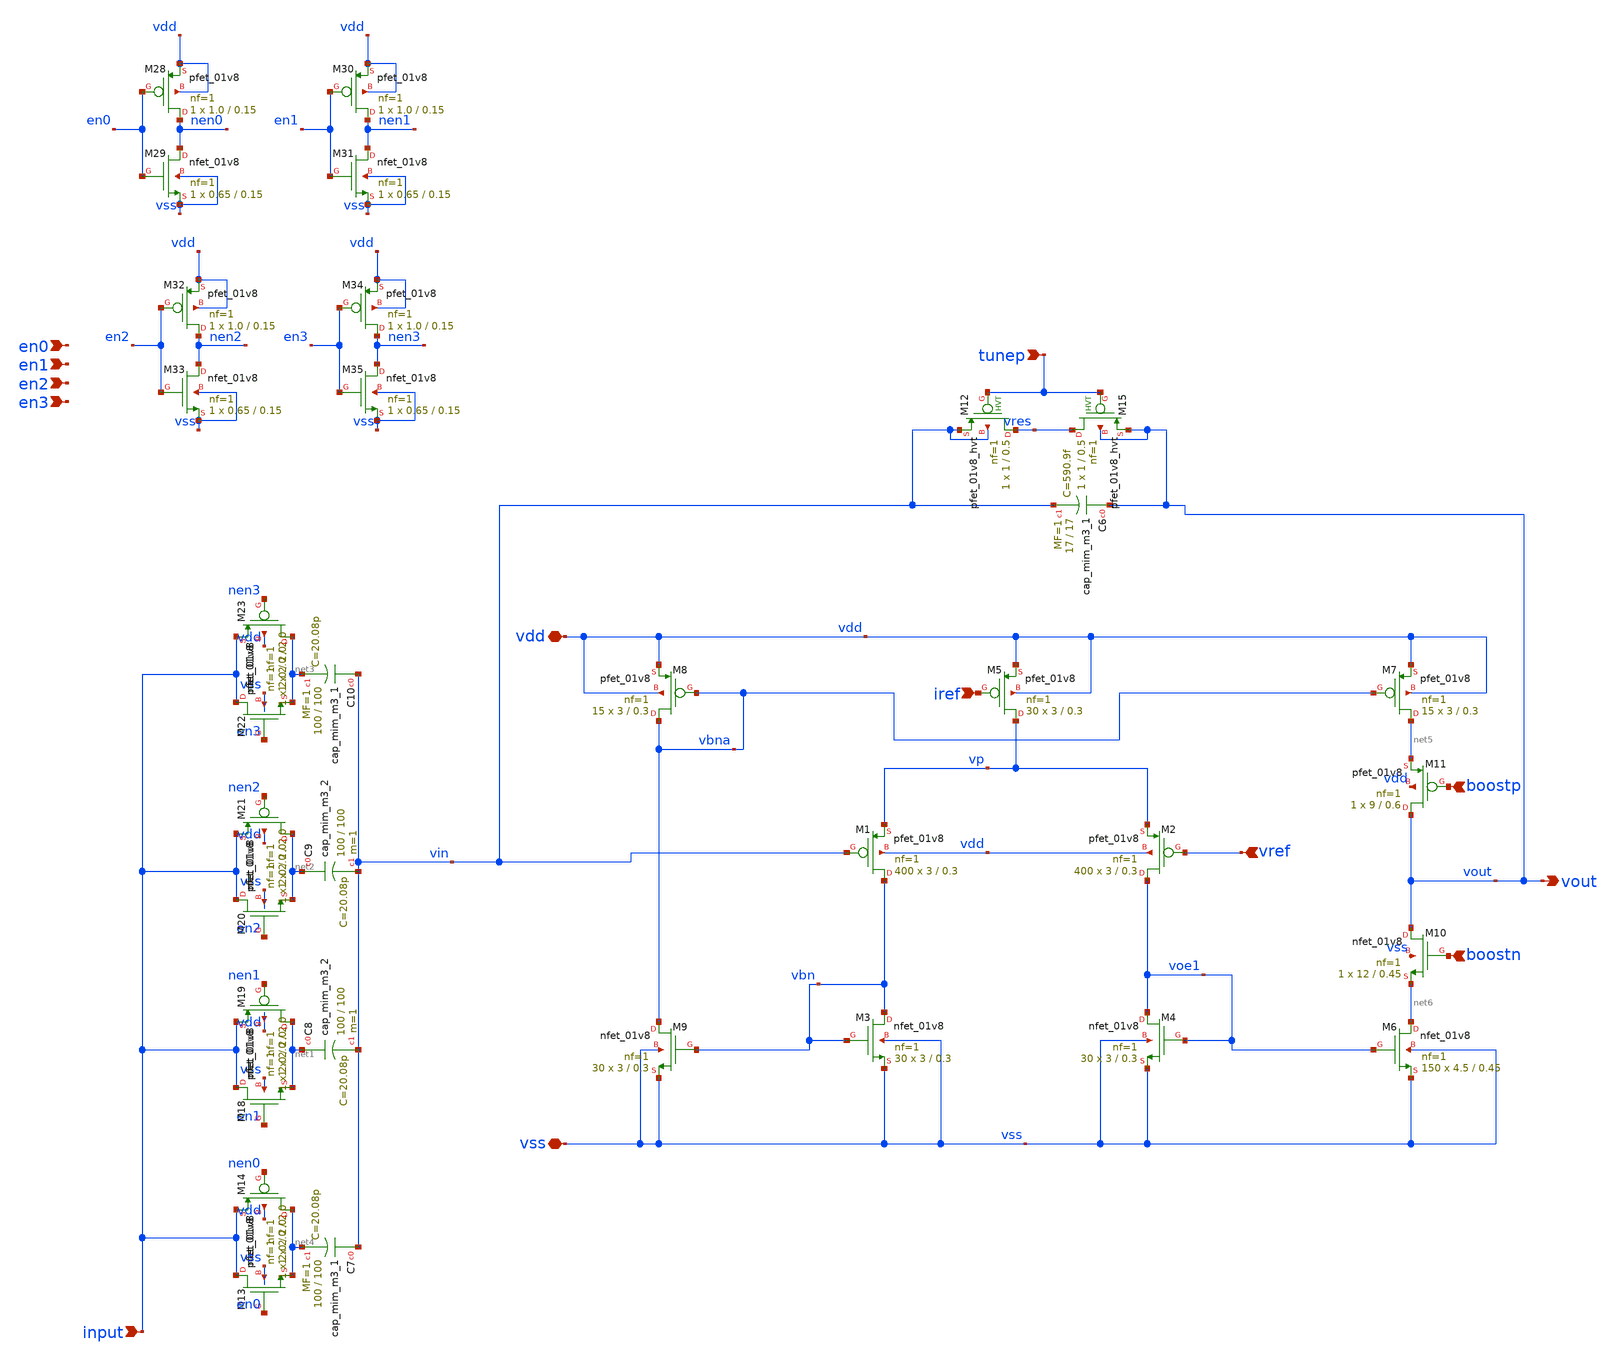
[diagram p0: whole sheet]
** sch_path: design/xschem/low_noise_amp_fc_v2.sch
**.subckt low_noise_amp_fc_v2 vdd vss vref vout iref en0 en1 en2 en3 input tunep boostp boostn
*.iopin vdd
*.iopin vss
*.ipin vref
*.opin vout
*.ipin iref
*.ipin en0
*.ipin en1
*.ipin en2
*.ipin en3
*.ipin input
*.ipin tunep
*.ipin boostp
*.ipin boostn
XM1 vbn vin vp vdd sky130_fd_pr__pfet_01v8 L=0.3 W=3 nf=1 ad='W * 0.29' as='W * 0.29' pd='2 * (W + 0.29)'
+ ps='2 * (W + 0.29)' nrd='0.29 / W' nrs='0.29 / W' sa=0 sb=0 sd=0 mult=400 m=400
XM2 voe1 vref vp vdd sky130_fd_pr__pfet_01v8 L=0.3 W=3 nf=1 ad='W * 0.29' as='W * 0.29' pd='2 * (W + 0.29)'
+ ps='2 * (W + 0.29)' nrd='0.29 / W' nrs='0.29 / W' sa=0 sb=0 sd=0 mult=400 m=400
XM3 vbn vbn vss vss sky130_fd_pr__nfet_01v8 L=0.3 W=3 nf=1 ad='W * 0.29' as='W * 0.29' pd='2 * (W + 0.29)'
+ ps='2 * (W + 0.29)' nrd='0.29 / W' nrs='0.29 / W' sa=0 sb=0 sd=0 mult=30 m=30
XM4 voe1 voe1 vss vss sky130_fd_pr__nfet_01v8 L=0.3 W=3 nf=1 ad='W * 0.29' as='W * 0.29' pd='2 * (W + 0.29)'
+ ps='2 * (W + 0.29)' nrd='0.29 / W' nrs='0.29 / W' sa=0 sb=0 sd=0 mult=30 m=30
XM5 vp iref vdd vdd sky130_fd_pr__pfet_01v8 L=0.3 W=3 nf=1 ad='W * 0.29' as='W * 0.29' pd='2 * (W + 0.29)'
+ ps='2 * (W + 0.29)' nrd='0.29 / W' nrs='0.29 / W' sa=0 sb=0 sd=0 mult=30 m=30
XM7 net5 vbna vdd vdd sky130_fd_pr__pfet_01v8 L=0.3 W=3 nf=1 ad='W * 0.29' as='W * 0.29' pd='2 * (W + 0.29)'
+ ps='2 * (W + 0.29)' nrd='0.29 / W' nrs='0.29 / W' sa=0 sb=0 sd=0 mult=15 m=15
XM8 vbna vbna vdd vdd sky130_fd_pr__pfet_01v8 L=0.3 W=3 nf=1 ad='W * 0.29' as='W * 0.29' pd='2 * (W + 0.29)'
+ ps='2 * (W + 0.29)' nrd='0.29 / W' nrs='0.29 / W' sa=0 sb=0 sd=0 mult=15 m=15
XM6 net6 voe1 vss vss sky130_fd_pr__nfet_01v8 L=0.45 W=4.5 nf=1 ad='W * 0.29' as='W * 0.29' pd='2 * (W + 0.29)'
+ ps='2 * (W + 0.29)' nrd='0.29 / W' nrs='0.29 / W' sa=0 sb=0 sd=0 mult=150 m=150
XM9 vbna vbn vss vss sky130_fd_pr__nfet_01v8 L=0.3 W=3 nf=1 ad='W * 0.29' as='W * 0.29' pd='2 * (W + 0.29)'
+ ps='2 * (W + 0.29)' nrd='0.29 / W' nrs='0.29 / W' sa=0 sb=0 sd=0 mult=30 m=30
XM28 nen0 en0 vdd vdd sky130_fd_pr__pfet_01v8 L=0.15 W=1.0 nf=1 ad='int((nf+1)/2) * W/nf * 0.29' as='int((nf+2)/2) * W/nf * 0.29'
+ pd='2*int((nf+1)/2) * (W/nf + 0.29)' ps='2*int((nf+2)/2) * (W/nf + 0.29)' nrd='0.29 / W' nrs='0.29 / W'
+ sa=0 sb=0 sd=0 mult=1 m=1
XM29 nen0 en0 vss vss sky130_fd_pr__nfet_01v8 L=0.15 W=0.65 nf=1 ad='int((nf+1)/2) * W/nf * 0.29' as='int((nf+2)/2) * W/nf * 0.29'
+ pd='2*int((nf+1)/2) * (W/nf + 0.29)' ps='2*int((nf+2)/2) * (W/nf + 0.29)' nrd='0.29 / W' nrs='0.29 / W'
+ sa=0 sb=0 sd=0 mult=1 m=1
XM30 nen1 en1 vdd vdd sky130_fd_pr__pfet_01v8 L=0.15 W=1.0 nf=1 ad='int((nf+1)/2) * W/nf * 0.29' as='int((nf+2)/2) * W/nf * 0.29'
+ pd='2*int((nf+1)/2) * (W/nf + 0.29)' ps='2*int((nf+2)/2) * (W/nf + 0.29)' nrd='0.29 / W' nrs='0.29 / W'
+ sa=0 sb=0 sd=0 mult=1 m=1
XM31 nen1 en1 vss vss sky130_fd_pr__nfet_01v8 L=0.15 W=0.65 nf=1 ad='int((nf+1)/2) * W/nf * 0.29' as='int((nf+2)/2) * W/nf * 0.29'
+ pd='2*int((nf+1)/2) * (W/nf + 0.29)' ps='2*int((nf+2)/2) * (W/nf + 0.29)' nrd='0.29 / W' nrs='0.29 / W'
+ sa=0 sb=0 sd=0 mult=1 m=1
XM32 nen2 en2 vdd vdd sky130_fd_pr__pfet_01v8 L=0.15 W=1.0 nf=1 ad='int((nf+1)/2) * W/nf * 0.29' as='int((nf+2)/2) * W/nf * 0.29'
+ pd='2*int((nf+1)/2) * (W/nf + 0.29)' ps='2*int((nf+2)/2) * (W/nf + 0.29)' nrd='0.29 / W' nrs='0.29 / W'
+ sa=0 sb=0 sd=0 mult=1 m=1
XM33 nen2 en2 vss vss sky130_fd_pr__nfet_01v8 L=0.15 W=0.65 nf=1 ad='int((nf+1)/2) * W/nf * 0.29' as='int((nf+2)/2) * W/nf * 0.29'
+ pd='2*int((nf+1)/2) * (W/nf + 0.29)' ps='2*int((nf+2)/2) * (W/nf + 0.29)' nrd='0.29 / W' nrs='0.29 / W'
+ sa=0 sb=0 sd=0 mult=1 m=1
XM34 nen3 en3 vdd vdd sky130_fd_pr__pfet_01v8 L=0.15 W=1.0 nf=1 ad='int((nf+1)/2) * W/nf * 0.29' as='int((nf+2)/2) * W/nf * 0.29'
+ pd='2*int((nf+1)/2) * (W/nf + 0.29)' ps='2*int((nf+2)/2) * (W/nf + 0.29)' nrd='0.29 / W' nrs='0.29 / W'
+ sa=0 sb=0 sd=0 mult=1 m=1
XM35 nen3 en3 vss vss sky130_fd_pr__nfet_01v8 L=0.15 W=0.65 nf=1 ad='int((nf+1)/2) * W/nf * 0.29' as='int((nf+2)/2) * W/nf * 0.29'
+ pd='2*int((nf+1)/2) * (W/nf + 0.29)' ps='2*int((nf+2)/2) * (W/nf + 0.29)' nrd='0.29 / W' nrs='0.29 / W'
+ sa=0 sb=0 sd=0 mult=1 m=1
XC7 vin net4 sky130_fd_pr__cap_mim_m3_1 W=100 L=100 MF=1 m=1
XC8 net1 vin sky130_fd_pr__cap_mim_m3_2 W=100 L=100 MF=1 m=1
XC9 net2 vin sky130_fd_pr__cap_mim_m3_2 W=100 L=100 MF=1 m=1
XC10 vin net3 sky130_fd_pr__cap_mim_m3_1 W=100 L=100 MF=1 m=1
XM13 input en0 net4 vss sky130_fd_pr__nfet_01v8 L=2.0 W=2.0 nf=1 ad='int((nf+1)/2) * W/nf * 0.29' as='int((nf+2)/2) * W/nf * 0.29'
+ pd='2*int((nf+1)/2) * (W/nf + 0.29)' ps='2*int((nf+2)/2) * (W/nf + 0.29)' nrd='0.29 / W' nrs='0.29 / W'
+ sa=0 sb=0 sd=0 mult=1 m=1
XM14 net4 nen0 input vdd sky130_fd_pr__pfet_01v8 L=2.0 W=2.0 nf=1 ad='int((nf+1)/2) * W/nf * 0.29' as='int((nf+2)/2) * W/nf * 0.29'
+ pd='2*int((nf+1)/2) * (W/nf + 0.29)' ps='2*int((nf+2)/2) * (W/nf + 0.29)' nrd='0.29 / W' nrs='0.29 / W'
+ sa=0 sb=0 sd=0 mult=1 m=1
XM18 input en1 net1 vss sky130_fd_pr__nfet_01v8 L=2.0 W=2.0 nf=1 ad='int((nf+1)/2) * W/nf * 0.29' as='int((nf+2)/2) * W/nf * 0.29'
+ pd='2*int((nf+1)/2) * (W/nf + 0.29)' ps='2*int((nf+2)/2) * (W/nf + 0.29)' nrd='0.29 / W' nrs='0.29 / W'
+ sa=0 sb=0 sd=0 mult=1 m=1
XM19 net1 nen1 input vdd sky130_fd_pr__pfet_01v8 L=2.0 W=2.0 nf=1 ad='int((nf+1)/2) * W/nf * 0.29' as='int((nf+2)/2) * W/nf * 0.29'
+ pd='2*int((nf+1)/2) * (W/nf + 0.29)' ps='2*int((nf+2)/2) * (W/nf + 0.29)' nrd='0.29 / W' nrs='0.29 / W'
+ sa=0 sb=0 sd=0 mult=1 m=1
XM20 input en2 net2 vss sky130_fd_pr__nfet_01v8 L=2.0 W=2.0 nf=1 ad='int((nf+1)/2) * W/nf * 0.29' as='int((nf+2)/2) * W/nf * 0.29'
+ pd='2*int((nf+1)/2) * (W/nf + 0.29)' ps='2*int((nf+2)/2) * (W/nf + 0.29)' nrd='0.29 / W' nrs='0.29 / W'
+ sa=0 sb=0 sd=0 mult=1 m=1
XM21 net2 nen2 input vdd sky130_fd_pr__pfet_01v8 L=2.0 W=2.0 nf=1 ad='int((nf+1)/2) * W/nf * 0.29' as='int((nf+2)/2) * W/nf * 0.29'
+ pd='2*int((nf+1)/2) * (W/nf + 0.29)' ps='2*int((nf+2)/2) * (W/nf + 0.29)' nrd='0.29 / W' nrs='0.29 / W'
+ sa=0 sb=0 sd=0 mult=1 m=1
XM22 input en3 net3 vss sky130_fd_pr__nfet_01v8 L=2.0 W=2.0 nf=1 ad='int((nf+1)/2) * W/nf * 0.29' as='int((nf+2)/2) * W/nf * 0.29'
+ pd='2*int((nf+1)/2) * (W/nf + 0.29)' ps='2*int((nf+2)/2) * (W/nf + 0.29)' nrd='0.29 / W' nrs='0.29 / W'
+ sa=0 sb=0 sd=0 mult=1 m=1
XM23 net3 nen3 input vdd sky130_fd_pr__pfet_01v8 L=2.0 W=2.0 nf=1 ad='int((nf+1)/2) * W/nf * 0.29' as='int((nf+2)/2) * W/nf * 0.29'
+ pd='2*int((nf+1)/2) * (W/nf + 0.29)' ps='2*int((nf+2)/2) * (W/nf + 0.29)' nrd='0.29 / W' nrs='0.29 / W'
+ sa=0 sb=0 sd=0 mult=1 m=1
XC6 vout vin sky130_fd_pr__cap_mim_m3_1 W=17 L=17 MF=1 m=1
XM10 vout boostn net6 vss sky130_fd_pr__nfet_01v8 L=0.45 W=12 nf=1 ad='W * 0.29' as='W * 0.29' pd='2 * (W + 0.29)'
+ ps='2 * (W + 0.29)' nrd='0.29 / W' nrs='0.29 / W' sa=0 sb=0 sd=0 mult=1 m=1
XM11 vout boostp net5 vdd sky130_fd_pr__pfet_01v8 L=0.6 W=9 nf=1 ad='W * 0.29' as='W * 0.29' pd='2 * (W + 0.29)'
+ ps='2 * (W + 0.29)' nrd='0.29 / W' nrs='0.29 / W' sa=0 sb=0 sd=0 mult=1 m=1
XM12 vres tunep vin vin sky130_fd_pr__pfet_01v8_hvt L=0.5 W=1 nf=1 ad='int((nf+1)/2) * W/nf * 0.29' as='int((nf+2)/2) * W/nf * 0.29'
+ pd='2*int((nf+1)/2) * (W/nf + 0.29)' ps='2*int((nf+2)/2) * (W/nf + 0.29)' nrd='0.29 / W' nrs='0.29 / W'
+ sa=0 sb=0 sd=0 mult=1 m=1
XM15 vres tunep vout vout sky130_fd_pr__pfet_01v8_hvt L=0.5 W=1 nf=1 ad='int((nf+1)/2) * W/nf * 0.29'
+ as='int((nf+2)/2) * W/nf * 0.29' pd='2*int((nf+1)/2) * (W/nf + 0.29)' ps='2*int((nf+2)/2) * (W/nf + 0.29)'
+ nrd='0.29 / W' nrs='0.29 / W' sa=0 sb=0 sd=0 mult=1 m=1
**.ends
.end
